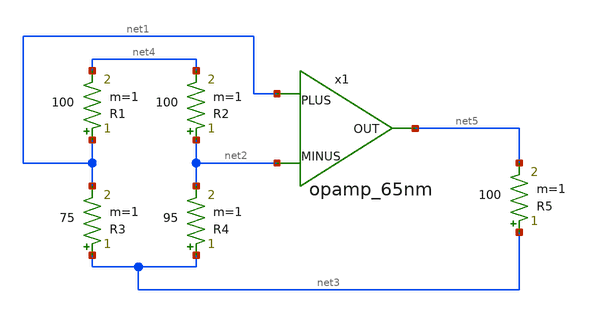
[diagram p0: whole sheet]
** sch_path: designs/wheatstone.sch
**.subckt wheatstone
R1 net1 net4 100 m=1
R2 net2 net4 100 m=1
R3 net3 net1 75 m=1
R4 net3 net2 95 m=1
x1 net1 net5 net2 opamp_65nm
R5 net3 net5 100 m=1
**.ends

* expanding   symbol:  opamp_65nm.sym # of pins=3
** sym_path: opamp_65nm.sym
** sch_path: opamp_65nm.sch
.subckt opamp_65nm PLUS OUT MINUS
*.ipin PLUS
*.ipin MINUS
*.opin OUT
M1 net1 GN1 0 0 nmos w=4u l=0.4u m=1
M2 GN1 GN1 0 0 nmos w=4u l=0.4u m=1
I0 VCC GN1 30u
M3 net2 MINUS net1 0 nmos w=1.5u l=0.2u m=1
M4 net3 PLUS net1 0 nmos w=1.5u l=0.2u m=1
M5 net2 net2 VCC VCC pmos w=6u l=0.3u m=1
M6 net3 net2 VCC VCC pmos w=6u l=0.3u m=1
M8 OUT net3 VCC VCC pmos w=6u l=0.4u m=1
.save v(gn1)
.save v(net2)
M7 OUT GN1 0 0 nmos w=4u l=0.4u m=1
R1 OUT net4 30k m=1
C1 net3 net4 150f m=1
C2 GN1 0 200f m=1
.save v(net1)
.ends

.end
